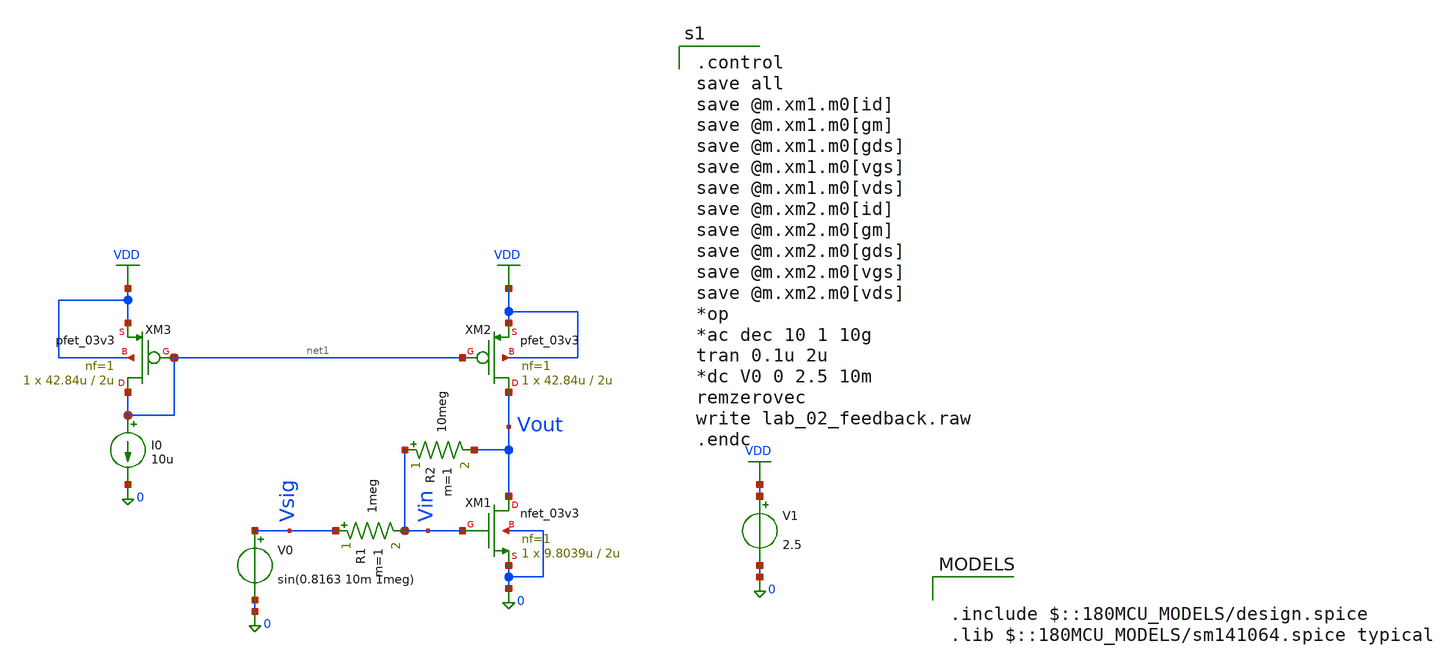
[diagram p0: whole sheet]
** sch_path: Lab_02/Lab_02_feedback.sch
**.subckt Lab_02_feedback
V1 VDD 0 2.5
XM1 Vout Vin 0 0 nfet_03v3 L=2u W=9.8039u nf=1 ad='int((nf+1)/2) * W/nf * 0.18u' as='int((nf+2)/2) * W/nf * 0.18u'
+ pd='2*int((nf+1)/2) * (W/nf + 0.18u)' ps='2*int((nf+2)/2) * (W/nf + 0.18u)' nrd='0.18u / W' nrs='0.18u / W'
+ sa=0 sb=0 sd=0 m=1
V0 Vsig 0 sin(0.8163 10m 1meg)
R1 Vsig Vin 1meg m=1
R2 Vin Vout 10meg m=1
XM2 Vout net1 VDD VDD pfet_03v3 L=2u W=42.84u nf=1 ad='int((nf+1)/2) * W/nf * 0.18u' as='int((nf+2)/2) * W/nf * 0.18u'
+ pd='2*int((nf+1)/2) * (W/nf + 0.18u)' ps='2*int((nf+2)/2) * (W/nf + 0.18u)' nrd='0.18u / W' nrs='0.18u / W'
+ sa=0 sb=0 sd=0 m=1
XM3 net1 net1 VDD VDD pfet_03v3 L=2u W=42.84u nf=1 ad='int((nf+1)/2) * W/nf * 0.18u' as='int((nf+2)/2) * W/nf * 0.18u'
+ pd='2*int((nf+1)/2) * (W/nf + 0.18u)' ps='2*int((nf+2)/2) * (W/nf + 0.18u)' nrd='0.18u / W' nrs='0.18u / W'
+ sa=0 sb=0 sd=0 m=1
I0 net1 0 10u
**** begin user architecture code

.control
save all
save @m.xm1.m0[id]
save @m.xm1.m0[gm]
save @m.xm1.m0[gds]
save @m.xm1.m0[vgs]
save @m.xm1.m0[vds]
save @m.xm2.m0[id]
save @m.xm2.m0[gm]
save @m.xm2.m0[gds]
save @m.xm2.m0[vgs]
save @m.xm2.m0[vds]
*op
*ac dec 10 1 10g
tran 0.1u 2u
*dc V0 0 2.5 10m
remzerovec
write lab_02_feedback.raw
.endc


.include $::180MCU_MODELS/design.spice
.lib $::180MCU_MODELS/sm141064.spice typical

**** end user architecture code
**.ends
.GLOBAL VDD
.end
